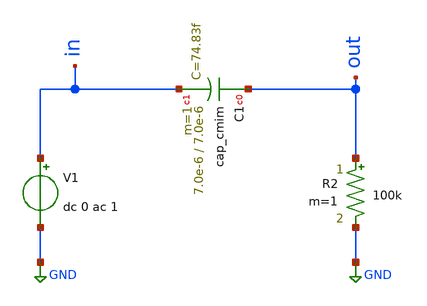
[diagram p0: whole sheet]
** sch_path: ihp-sg13g2/xschem_libs/sg13g2_tests_ase/mc_mim_cap_ac/schematic/mc_mim_cap_ac.sch
* Copyright 2021 Stefan Frederik Schippers
* Licensed under the Apache License, Version 2.0 (the "License");
* you may not use this file except in compliance with the License.
* You may obtain a copy of the License at
* https://www.apache.org/licenses/LICENSE-2.0
* Unless required by applicable law or agreed to in writing, software
* distributed under the License is distributed on an "AS IS" BASIS,
* WITHOUT WARRANTIES OR CONDITIONS OF ANY KIND, either express or implied.
* See the License for the specific language governing permissions and
* limitations under the License.
* Copyright 2023 IHP PDK Authors
**.subckt mc_mim_cap_ac
V1 in GND dc 0 ac 1
R2 out GND 100k m=1
XC1 out in cap_cmim w=7.0e-6 l=7.0e-6 m=1 mm_ok=1
**.ends
.GLOBAL GND
.end
